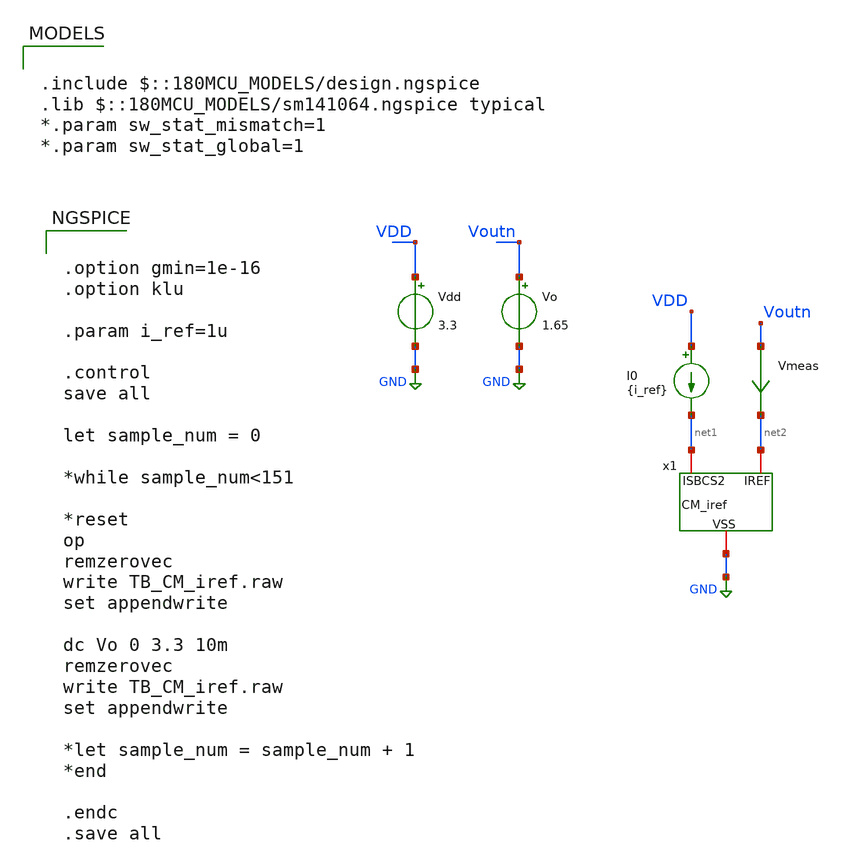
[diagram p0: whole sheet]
** sch_path: TIA_Filter/CurrentMirrors/TB_CM_iref.sch
**.subckt TB_CM_iref
Vdd VDD GND 3.3
Vo Voutn GND 1.65
x1 net1 net2 GND CM_iref
I0 VDD net1 {i_ref}
Vmeas Voutn net2 0
.save i(vmeas)
**** begin user architecture code


.option gmin=1e-16
.option klu

.param i_ref=1u

.control
save all

let sample_num = 0

*while sample_num<151

*reset
op
remzerovec
write TB_CM_iref.raw
set appendwrite

dc Vo 0 3.3 10m
remzerovec
write TB_CM_iref.raw
set appendwrite

*let sample_num = sample_num + 1
*end

.endc
.save all



.include $::180MCU_MODELS/design.ngspice
.lib $::180MCU_MODELS/sm141064.ngspice typical
*.param sw_stat_mismatch=1
*.param sw_stat_global=1

**** end user architecture code
**.ends

* expanding   symbol:  CurrentMirrors/CM_iref.sym # of pins=3
** sym_path: TIA_Filter/CurrentMirrors/CM_iref.sym
** sch_path: TIA_Filter/CurrentMirrors/CM_iref.sch
.subckt CM_iref ISBCS2 IREF VSS
*.iopin ISBCS2
*.iopin IREF
*.iopin VSS
XM6 ISBCS2 ISBCS2 VSS VSS nfet_03v3 L=6u W=2u nf=1 ad='int((nf+1)/2) * W/nf * 0.18u' as='int((nf+2)/2) * W/nf * 0.18u'
+ pd='2*int((nf+1)/2) * (W/nf + 0.18u)' ps='2*int((nf+2)/2) * (W/nf + 0.18u)' nrd='0.18u / W' nrs='0.18u / W'
+ sa=0 sb=0 sd=0 m=1
XM5 IREF ISBCS2 net3 VSS nfet_03v3 L=6u W=2u nf=1 ad='int((nf+1)/2) * W/nf * 0.18u' as='int((nf+2)/2) * W/nf * 0.18u'
+ pd='2*int((nf+1)/2) * (W/nf + 0.18u)' ps='2*int((nf+2)/2) * (W/nf + 0.18u)' nrd='0.18u / W' nrs='0.18u / W'
+ sa=0 sb=0 sd=0 m=1
XM1 net3 ISBCS2 net2 VSS nfet_03v3 L=6u W=2u nf=1 ad='int((nf+1)/2) * W/nf * 0.18u' as='int((nf+2)/2) * W/nf * 0.18u'
+ pd='2*int((nf+1)/2) * (W/nf + 0.18u)' ps='2*int((nf+2)/2) * (W/nf + 0.18u)' nrd='0.18u / W' nrs='0.18u / W'
+ sa=0 sb=0 sd=0 m=1
XM2 net2 ISBCS2 net1 VSS nfet_03v3 L=6u W=2u nf=1 ad='int((nf+1)/2) * W/nf * 0.18u' as='int((nf+2)/2) * W/nf * 0.18u'
+ pd='2*int((nf+1)/2) * (W/nf + 0.18u)' ps='2*int((nf+2)/2) * (W/nf + 0.18u)' nrd='0.18u / W' nrs='0.18u / W'
+ sa=0 sb=0 sd=0 m=1
XM3 net1 ISBCS2 net4 VSS nfet_03v3 L=6u W=2u nf=1 ad='int((nf+1)/2) * W/nf * 0.18u' as='int((nf+2)/2) * W/nf * 0.18u'
+ pd='2*int((nf+1)/2) * (W/nf + 0.18u)' ps='2*int((nf+2)/2) * (W/nf + 0.18u)' nrd='0.18u / W' nrs='0.18u / W'
+ sa=0 sb=0 sd=0 m=1
XM4 net4 ISBCS2 VSS VSS nfet_03v3 L=6u W=2u nf=1 ad='int((nf+1)/2) * W/nf * 0.18u' as='int((nf+2)/2) * W/nf * 0.18u'
+ pd='2*int((nf+1)/2) * (W/nf + 0.18u)' ps='2*int((nf+2)/2) * (W/nf + 0.18u)' nrd='0.18u / W' nrs='0.18u / W'
+ sa=0 sb=0 sd=0 m=1
XM7[1] VSS VSS VSS VSS nfet_03v3 L=6u W=2u nf=1 ad='int((nf+1)/2) * W/nf * 0.18u' as='int((nf+2)/2) * W/nf * 0.18u'
+ pd='2*int((nf+1)/2) * (W/nf + 0.18u)' ps='2*int((nf+2)/2) * (W/nf + 0.18u)' nrd='0.18u / W' nrs='0.18u / W'
+ sa=0 sb=0 sd=0 m=1
XM7[2] VSS VSS VSS VSS nfet_03v3 L=6u W=2u nf=1 ad='int((nf+1)/2) * W/nf * 0.18u' as='int((nf+2)/2) * W/nf * 0.18u'
+ pd='2*int((nf+1)/2) * (W/nf + 0.18u)' ps='2*int((nf+2)/2) * (W/nf + 0.18u)' nrd='0.18u / W' nrs='0.18u / W'
+ sa=0 sb=0 sd=0 m=1
XM7[3] VSS VSS VSS VSS nfet_03v3 L=6u W=2u nf=1 ad='int((nf+1)/2) * W/nf * 0.18u' as='int((nf+2)/2) * W/nf * 0.18u'
+ pd='2*int((nf+1)/2) * (W/nf + 0.18u)' ps='2*int((nf+2)/2) * (W/nf + 0.18u)' nrd='0.18u / W' nrs='0.18u / W'
+ sa=0 sb=0 sd=0 m=1
XM7[4] VSS VSS VSS VSS nfet_03v3 L=6u W=2u nf=1 ad='int((nf+1)/2) * W/nf * 0.18u' as='int((nf+2)/2) * W/nf * 0.18u'
+ pd='2*int((nf+1)/2) * (W/nf + 0.18u)' ps='2*int((nf+2)/2) * (W/nf + 0.18u)' nrd='0.18u / W' nrs='0.18u / W'
+ sa=0 sb=0 sd=0 m=1
XM7[5] VSS VSS VSS VSS nfet_03v3 L=6u W=2u nf=1 ad='int((nf+1)/2) * W/nf * 0.18u' as='int((nf+2)/2) * W/nf * 0.18u'
+ pd='2*int((nf+1)/2) * (W/nf + 0.18u)' ps='2*int((nf+2)/2) * (W/nf + 0.18u)' nrd='0.18u / W' nrs='0.18u / W'
+ sa=0 sb=0 sd=0 m=1
XM7[6] VSS VSS VSS VSS nfet_03v3 L=6u W=2u nf=1 ad='int((nf+1)/2) * W/nf * 0.18u' as='int((nf+2)/2) * W/nf * 0.18u'
+ pd='2*int((nf+1)/2) * (W/nf + 0.18u)' ps='2*int((nf+2)/2) * (W/nf + 0.18u)' nrd='0.18u / W' nrs='0.18u / W'
+ sa=0 sb=0 sd=0 m=1
XM7[7] VSS VSS VSS VSS nfet_03v3 L=6u W=2u nf=1 ad='int((nf+1)/2) * W/nf * 0.18u' as='int((nf+2)/2) * W/nf * 0.18u'
+ pd='2*int((nf+1)/2) * (W/nf + 0.18u)' ps='2*int((nf+2)/2) * (W/nf + 0.18u)' nrd='0.18u / W' nrs='0.18u / W'
+ sa=0 sb=0 sd=0 m=1
XM7[8] VSS VSS VSS VSS nfet_03v3 L=6u W=2u nf=1 ad='int((nf+1)/2) * W/nf * 0.18u' as='int((nf+2)/2) * W/nf * 0.18u'
+ pd='2*int((nf+1)/2) * (W/nf + 0.18u)' ps='2*int((nf+2)/2) * (W/nf + 0.18u)' nrd='0.18u / W' nrs='0.18u / W'
+ sa=0 sb=0 sd=0 m=1
XM7[9] VSS VSS VSS VSS nfet_03v3 L=6u W=2u nf=1 ad='int((nf+1)/2) * W/nf * 0.18u' as='int((nf+2)/2) * W/nf * 0.18u'
+ pd='2*int((nf+1)/2) * (W/nf + 0.18u)' ps='2*int((nf+2)/2) * (W/nf + 0.18u)' nrd='0.18u / W' nrs='0.18u / W'
+ sa=0 sb=0 sd=0 m=1
XM7[10] VSS VSS VSS VSS nfet_03v3 L=6u W=2u nf=1 ad='int((nf+1)/2) * W/nf * 0.18u' as='int((nf+2)/2) * W/nf * 0.18u'
+ pd='2*int((nf+1)/2) * (W/nf + 0.18u)' ps='2*int((nf+2)/2) * (W/nf + 0.18u)' nrd='0.18u / W' nrs='0.18u / W'
+ sa=0 sb=0 sd=0 m=1
XM7[11] VSS VSS VSS VSS nfet_03v3 L=6u W=2u nf=1 ad='int((nf+1)/2) * W/nf * 0.18u' as='int((nf+2)/2) * W/nf * 0.18u'
+ pd='2*int((nf+1)/2) * (W/nf + 0.18u)' ps='2*int((nf+2)/2) * (W/nf + 0.18u)' nrd='0.18u / W' nrs='0.18u / W'
+ sa=0 sb=0 sd=0 m=1
XM7[12] VSS VSS VSS VSS nfet_03v3 L=6u W=2u nf=1 ad='int((nf+1)/2) * W/nf * 0.18u' as='int((nf+2)/2) * W/nf * 0.18u'
+ pd='2*int((nf+1)/2) * (W/nf + 0.18u)' ps='2*int((nf+2)/2) * (W/nf + 0.18u)' nrd='0.18u / W' nrs='0.18u / W'
+ sa=0 sb=0 sd=0 m=1
XM7[13] VSS VSS VSS VSS nfet_03v3 L=6u W=2u nf=1 ad='int((nf+1)/2) * W/nf * 0.18u' as='int((nf+2)/2) * W/nf * 0.18u'
+ pd='2*int((nf+1)/2) * (W/nf + 0.18u)' ps='2*int((nf+2)/2) * (W/nf + 0.18u)' nrd='0.18u / W' nrs='0.18u / W'
+ sa=0 sb=0 sd=0 m=1
XM7[14] VSS VSS VSS VSS nfet_03v3 L=6u W=2u nf=1 ad='int((nf+1)/2) * W/nf * 0.18u' as='int((nf+2)/2) * W/nf * 0.18u'
+ pd='2*int((nf+1)/2) * (W/nf + 0.18u)' ps='2*int((nf+2)/2) * (W/nf + 0.18u)' nrd='0.18u / W' nrs='0.18u / W'
+ sa=0 sb=0 sd=0 m=1
XM7[15] VSS VSS VSS VSS nfet_03v3 L=6u W=2u nf=1 ad='int((nf+1)/2) * W/nf * 0.18u' as='int((nf+2)/2) * W/nf * 0.18u'
+ pd='2*int((nf+1)/2) * (W/nf + 0.18u)' ps='2*int((nf+2)/2) * (W/nf + 0.18u)' nrd='0.18u / W' nrs='0.18u / W'
+ sa=0 sb=0 sd=0 m=1
XM7[16] VSS VSS VSS VSS nfet_03v3 L=6u W=2u nf=1 ad='int((nf+1)/2) * W/nf * 0.18u' as='int((nf+2)/2) * W/nf * 0.18u'
+ pd='2*int((nf+1)/2) * (W/nf + 0.18u)' ps='2*int((nf+2)/2) * (W/nf + 0.18u)' nrd='0.18u / W' nrs='0.18u / W'
+ sa=0 sb=0 sd=0 m=1
XM7[17] VSS VSS VSS VSS nfet_03v3 L=6u W=2u nf=1 ad='int((nf+1)/2) * W/nf * 0.18u' as='int((nf+2)/2) * W/nf * 0.18u'
+ pd='2*int((nf+1)/2) * (W/nf + 0.18u)' ps='2*int((nf+2)/2) * (W/nf + 0.18u)' nrd='0.18u / W' nrs='0.18u / W'
+ sa=0 sb=0 sd=0 m=1
XM7[18] VSS VSS VSS VSS nfet_03v3 L=6u W=2u nf=1 ad='int((nf+1)/2) * W/nf * 0.18u' as='int((nf+2)/2) * W/nf * 0.18u'
+ pd='2*int((nf+1)/2) * (W/nf + 0.18u)' ps='2*int((nf+2)/2) * (W/nf + 0.18u)' nrd='0.18u / W' nrs='0.18u / W'
+ sa=0 sb=0 sd=0 m=1
.ends

.GLOBAL GND
.end
